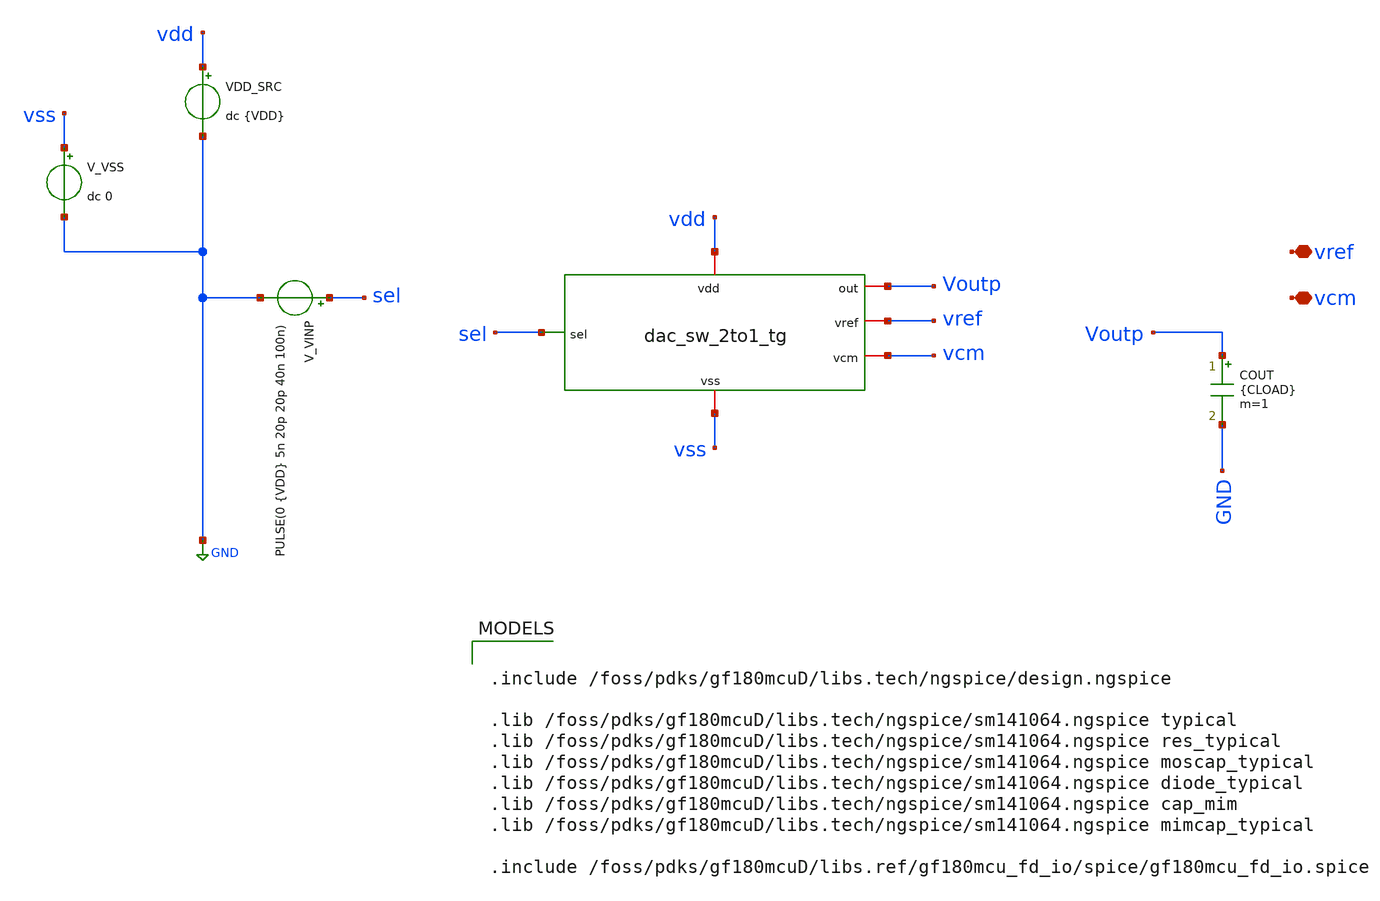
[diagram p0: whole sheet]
** sch_path: circuit_files/sar_adc_test/tb/dac_sw_tb.sch
**.subckt dac_sw_tb vref vcm
*.iopin vref
*.iopin vcm
x1 sel Voutp vss vdd vref vcm dac_sw_2to1_tg
VDD_SRC vdd GND dc {VDD}
V_VINP sel GND PULSE(0 {VDD} 5n 20p 20p 40n 100n)
V_VSS vss GND dc 0
COUT Voutp GND {CLOAD} m=1
**** begin user architecture code

.include /foss/pdks/gf180mcuD/libs.tech/ngspice/design.ngspice

.lib /foss/pdks/gf180mcuD/libs.tech/ngspice/sm141064.ngspice typical
.lib /foss/pdks/gf180mcuD/libs.tech/ngspice/sm141064.ngspice res_typical
.lib /foss/pdks/gf180mcuD/libs.tech/ngspice/sm141064.ngspice moscap_typical
.lib /foss/pdks/gf180mcuD/libs.tech/ngspice/sm141064.ngspice diode_typical
.lib /foss/pdks/gf180mcuD/libs.tech/ngspice/sm141064.ngspice cap_mim
.lib /foss/pdks/gf180mcuD/libs.tech/ngspice/sm141064.ngspice mimcap_typical

.include /foss/pdks/gf180mcuD/libs.ref/gf180mcu_fd_io/spice/gf180mcu_fd_io.spice




* ------------------------------------------------------------
* Parameters
* CLOAD = 25.6 pF approximates one MSB bottom-plate load:
* 512 * 50 fF = 25.6 pF
* ------------------------------------------------------------
.param VDD=3.3
.param VCM=1.65
.param VREF=3.3
.param VDIFF=0
.param CLOAD=25.6p

* ------------------------------------------------------------
* Local reference sources for this standalone testbench
* ------------------------------------------------------------
VREF_SRC vref GND dc {VREF}
VVCM_SRC vcm  GND dc {VCM}

* ------------------------------------------------------------
* Simulation options
* ------------------------------------------------------------
.options savecurrents
.options reltol=1e-4 abstol=1e-12 vntol=1e-6
.options method=gear maxord=2

* ------------------------------------------------------------
* Save useful nodes/currents
* ------------------------------------------------------------
.save v(sel)
.save v(Voutp)
.save v(vref)
.save v(vcm)
.save v(vdd)
.save v(vss)
.save i(VDD_SRC)
.save i(VREF_SRC)
.save i(VVCM_SRC)

.control

shell rm -f dac_sw_results.txt

echo ================================================== > dac_sw_results.txt
echo DAC SWITCH 2:1 TRANSMISSION-GATE VERIFICATION >> dac_sw_results.txt
echo ================================================== >> dac_sw_results.txt
echo Cell under test: dac_sw_2to1_tg >> dac_sw_results.txt
echo Expected function: sel=0 gives out=vcm, sel=1 gives out=vref >> dac_sw_results.txt
echo Selector source must be: PULSE(0 {VDD} 5n 20p 20p 40n 100n) >> dac_sw_results.txt
echo Load capacitance CLOAD = 25.6pF, approximately 512*50fF MSB CDAC load >> dac_sw_results.txt
echo Pass threshold for settled error = 5mV >> dac_sw_results.txt
echo ================================================== >> dac_sw_results.txt
echo columns: CASE vref_set sel_low out_low err_low sel_high out_high err_high sel_return out_return
+ err_return t_sel_rise t_out_to_ref tpd_to_ref t_sel_fall t_out_to_vcm tpd_to_vcm ivdd_avg ivref_avg ivcm_avg
+ pdd_avg pass_low pass_high pass_return >> dac_sw_results.txt
echo ================================================== >> dac_sw_results.txt


* ==================================================
* CASE A: vref = VDD = 3.3V
* Positive-side CDAC switch behavior
* sel=0 -> out=vcm=1.65V
* sel=1 -> out=vref=3.3V
* ==================================================

alterparam VREF = 3.3
reset
tran 2p 100n

meas tran sel_low_A    FIND v(sel)   AT=4n
meas tran out_low_A    FIND v(Voutp) AT=4n
meas tran vcm_A        FIND v(vcm)   AT=4n
let err_low_A = out_low_A - vcm_A

meas tran sel_high_A   FIND v(sel)   AT=20n
meas tran out_high_A   FIND v(Voutp) AT=20n
meas tran vref_A       FIND v(vref)  AT=20n
let err_high_A = out_high_A - vref_A

meas tran sel_ret_A    FIND v(sel)   AT=80n
meas tran out_ret_A    FIND v(Voutp) AT=80n
meas tran vcm_ret_A    FIND v(vcm)   AT=80n
let err_ret_A = out_ret_A - vcm_ret_A

* Rising select: output should rise from VCM to VREF.
* Midpoint = (1.65 + 3.3)/2 = 2.475V
meas tran t_sel_rise_A WHEN v(sel)=1.65 RISE=1
meas tran t_out_ref_A  WHEN v(Voutp)=2.475 RISE=1
let tpd_ref_A = t_out_ref_A - t_sel_rise_A

* Falling select: output should return from VREF to VCM.
meas tran t_sel_fall_A WHEN v(sel)=1.65 FALL=1
meas tran t_out_vcm_A  WHEN v(Voutp)=2.475 FALL=1
let tpd_vcm_A = t_out_vcm_A - t_sel_fall_A

meas tran ivdd_avg_A  AVG i(VDD_SRC)  FROM=0n TO=90n
meas tran ivref_avg_A AVG i(VREF_SRC) FROM=0n TO=90n
meas tran ivcm_avg_A  AVG i(VVCM_SRC) FROM=0n TO=90n
let pdd_avg_A = abs(3.3*ivdd_avg_A)

let pass_low_A = 0
if abs(err_low_A) < 5e-3
  let pass_low_A = 1
end

let pass_high_A = 0
if abs(err_high_A) < 5e-3
  let pass_high_A = 1
end

let pass_ret_A = 0
if abs(err_ret_A) < 5e-3
  let pass_ret_A = 1
end

echo REF_HIGH_3P3 $&vref_A $&sel_low_A $&out_low_A $&err_low_A $&sel_high_A $&out_high_A
+ $&err_high_A $&sel_ret_A $&out_ret_A $&err_ret_A $&t_sel_rise_A $&t_out_ref_A $&tpd_ref_A $&t_sel_fall_A
+ $&t_out_vcm_A $&tpd_vcm_A $&ivdd_avg_A $&ivref_avg_A $&ivcm_avg_A $&pdd_avg_A $&pass_low_A $&pass_high_A
+ $&pass_ret_A >> dac_sw_results.txt


* ==================================================
* CASE B: vref = VSS = 0V
* Negative-side CDAC switch behavior
* sel=0 -> out=vcm=1.65V
* sel=1 -> out=vref=0V
* ==================================================

alterparam VREF = 0
reset
tran 2p 100n

meas tran sel_low_B    FIND v(sel)   AT=4n
meas tran out_low_B    FIND v(Voutp) AT=4n
meas tran vcm_B        FIND v(vcm)   AT=4n
let err_low_B = out_low_B - vcm_B

meas tran sel_high_B   FIND v(sel)   AT=20n
meas tran out_high_B   FIND v(Voutp) AT=20n
meas tran vref_B       FIND v(vref)  AT=20n
let err_high_B = out_high_B - vref_B

meas tran sel_ret_B    FIND v(sel)   AT=80n
meas tran out_ret_B    FIND v(Voutp) AT=80n
meas tran vcm_ret_B    FIND v(vcm)   AT=80n
let err_ret_B = out_ret_B - vcm_ret_B

* Rising select: output should fall from VCM to VREF=0.
* Midpoint = (1.65 + 0)/2 = 0.825V
meas tran t_sel_rise_B WHEN v(sel)=1.65 RISE=1
meas tran t_out_ref_B  WHEN v(Voutp)=0.825 FALL=1
let tpd_ref_B = t_out_ref_B - t_sel_rise_B

* Falling select: output should return from VREF=0 to VCM.
meas tran t_sel_fall_B WHEN v(sel)=1.65 FALL=1
meas tran t_out_vcm_B  WHEN v(Voutp)=0.825 RISE=1
let tpd_vcm_B = t_out_vcm_B - t_sel_fall_B

meas tran ivdd_avg_B  AVG i(VDD_SRC)  FROM=0n TO=90n
meas tran ivref_avg_B AVG i(VREF_SRC) FROM=0n TO=90n
meas tran ivcm_avg_B  AVG i(VVCM_SRC) FROM=0n TO=90n
let pdd_avg_B = abs(3.3*ivdd_avg_B)

let pass_low_B = 0
if abs(err_low_B) < 5e-3
  let pass_low_B = 1
end

let pass_high_B = 0
if abs(err_high_B) < 5e-3
  let pass_high_B = 1
end

let pass_ret_B = 0
if abs(err_ret_B) < 5e-3
  let pass_ret_B = 1
end

echo REF_LOW_0 $&vref_B $&sel_low_B $&out_low_B $&err_low_B $&sel_high_B $&out_high_B $&err_high_B
+ $&sel_ret_B $&out_ret_B $&err_ret_B $&t_sel_rise_B $&t_out_ref_B $&tpd_ref_B $&t_sel_fall_B $&t_out_vcm_B
+ $&tpd_vcm_B $&ivdd_avg_B $&ivref_avg_B $&ivcm_avg_B $&pdd_avg_B $&pass_low_B $&pass_high_B $&pass_ret_B >>
+ dac_sw_results.txt


echo ================================================== >> dac_sw_results.txt
echo INTERPRETATION >> dac_sw_results.txt
echo pass_low=1 means sel=0 correctly connects out to VCM >> dac_sw_results.txt
echo pass_high=1 means sel=1 correctly connects out to VREF >> dac_sw_results.txt
echo pass_return=1 means falling sel correctly reconnects out to VCM >> dac_sw_results.txt
echo tpd_to_ref is delay from sel crossing 1.65V to output crossing midpoint toward VREF >>
+ dac_sw_results.txt
echo tpd_to_vcm is delay from sel crossing 1.65V to output crossing midpoint toward VCM >>
+ dac_sw_results.txt
echo REF_HIGH_3P3 validates positive CDAC bp switch behavior >> dac_sw_results.txt
echo REF_LOW_0 validates negative CDAC bn switch behavior >> dac_sw_results.txt
echo ================================================== >> dac_sw_results.txt

echo DAC switch test complete. Open dac_sw_results.txt.

write dac_sw_tb.raw

.endc


**** end user architecture code
**.ends

* expanding   symbol:  dac_sw_2to1_tg.sym # of pins=6
** sym_path: circuit_files/sar_adc_test/xschem/dac_sw_2to1_tg.sym
** sch_path: circuit_files/sar_adc_test/xschem/dac_sw_2to1_tg.sch
.subckt dac_sw_2to1_tg sel out vss vdd vref vcm
*.ipin sel
*.iopin vdd
*.iopin vref
*.iopin vcm
*.iopin vss
*.iopin out
x1 vss sel selb vdd vref out tg
x3 vss selb sel vdd vcm out tg
x2 vdd sel selb vss inverter
.ends


* expanding   symbol:  /home/arjun/eda/projects/SAR_ADC/circuit_files/sar_adc_test/xschem/tg.sym #
*+ of pins=6
** sym_path: circuit_files/sar_adc_test/xschem/tg.sym
** sch_path: circuit_files/sar_adc_test/xschem/tg.sch
.subckt tg vss ng pg vdd a b
*.ipin ng
*.iopin vdd
*.ipin pg
*.iopin a
*.iopin b
*.iopin vss
XM12 b ng a vss sg13_hv_nmos w=2u l=0.45u ng=1 m=1 mm_ok=1
XM16 b pg a vdd sg13_hv_pmos w=2u l=0.4u ng=1 m=2 mm_ok=1
.ends


* expanding   symbol:
*+  /home/arjun/eda/projects/SAR_ADC/circuit_files/sar_adc_test/xschem/inverter.sym # of pins=4
** sym_path: circuit_files/sar_adc_test/xschem/inverter.sym
** sch_path: circuit_files/sar_adc_test/xschem/inverter.sch
.subckt inverter vdd Vinn Voutp vss
*.iopin vdd
*.iopin vss
*.ipin Vinn
*.opin Voutp
XM12 Voutp Vinn vss vss sg13_hv_nmos w=2u l=0.45u ng=1 m=1 mm_ok=1
XM16 Voutp Vinn vdd vdd sg13_hv_pmos w=2u l=0.4u ng=1 m=2 mm_ok=1
.ends

.GLOBAL GND
.end
